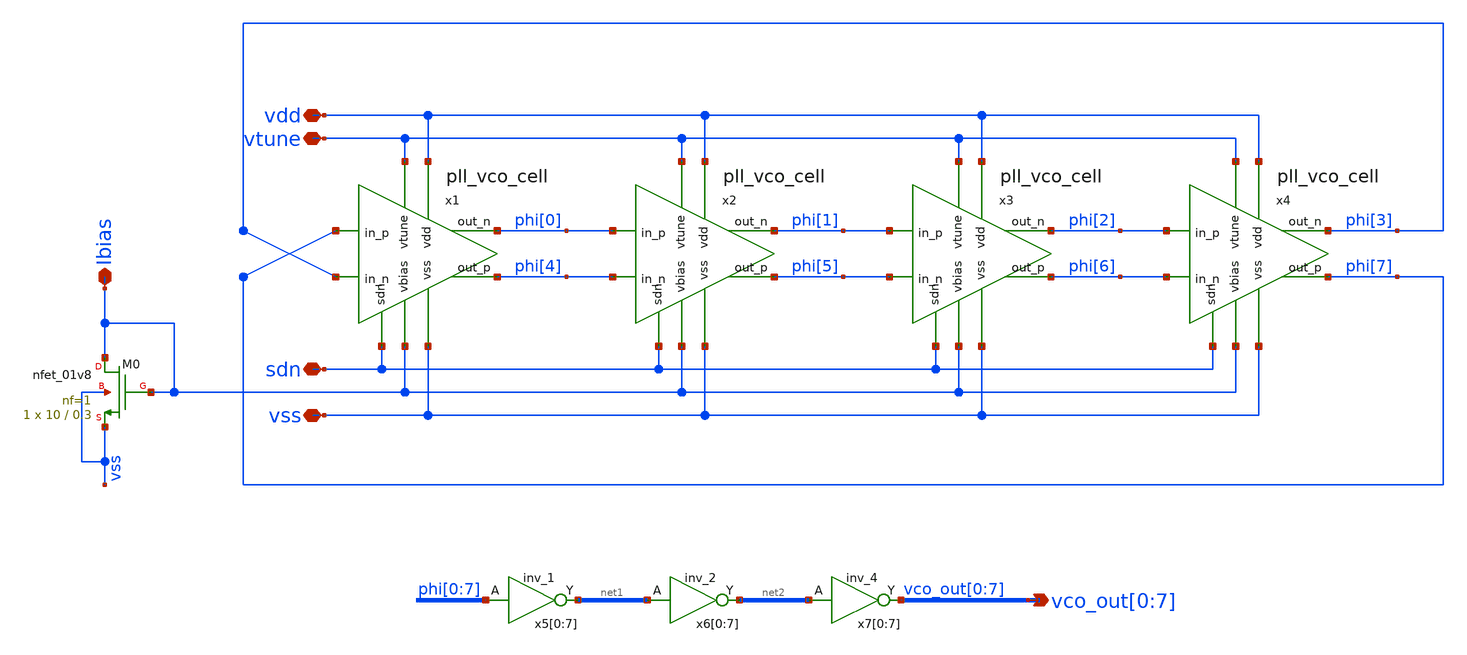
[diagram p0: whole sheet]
** sch_path: pll/pll_vco/xschem/pll_vco.sch
**.subckt pll_vco vss vdd vtune Ibias
*+ vco_out[0],vco_out[1],vco_out[2],vco_out[3],vco_out[4],vco_out[5],vco_out[6],vco_out[7] sdn
*.iopin vss
*.iopin vdd
*.iopin vtune
*.iopin Ibias
*.opin vco_out[0],vco_out[1],vco_out[2],vco_out[3],vco_out[4],vco_out[5],vco_out[6],vco_out[7]
*.iopin sdn
XM0 Ibias Ibias vss vss sky130_fd_pr__nfet_01v8 L=0.3 W=10 nf=1 ad='int((nf+1)/2) * W/nf * 0.29' as='int((nf+2)/2) * W/nf * 0.29'
+ pd='2*int((nf+1)/2) * (W/nf + 0.29)' ps='2*int((nf+2)/2) * (W/nf + 0.29)' nrd='0.29 / W' nrs='0.29 / W'
+ sa=0 sb=0 sd=0 mult=1 m=1
x5[0] phi[0] vss vss vdd vdd net1[7] sky130_fd_sc_hs__inv_1
x5[1] phi[1] vss vss vdd vdd net1[6] sky130_fd_sc_hs__inv_1
x5[2] phi[2] vss vss vdd vdd net1[5] sky130_fd_sc_hs__inv_1
x5[3] phi[3] vss vss vdd vdd net1[4] sky130_fd_sc_hs__inv_1
x5[4] phi[4] vss vss vdd vdd net1[3] sky130_fd_sc_hs__inv_1
x5[5] phi[5] vss vss vdd vdd net1[2] sky130_fd_sc_hs__inv_1
x5[6] phi[6] vss vss vdd vdd net1[1] sky130_fd_sc_hs__inv_1
x5[7] phi[7] vss vss vdd vdd net1[0] sky130_fd_sc_hs__inv_1
x6[0] net1[7] vss vss vdd vdd net2[7] sky130_fd_sc_hs__inv_2
x6[1] net1[6] vss vss vdd vdd net2[6] sky130_fd_sc_hs__inv_2
x6[2] net1[5] vss vss vdd vdd net2[5] sky130_fd_sc_hs__inv_2
x6[3] net1[4] vss vss vdd vdd net2[4] sky130_fd_sc_hs__inv_2
x6[4] net1[3] vss vss vdd vdd net2[3] sky130_fd_sc_hs__inv_2
x6[5] net1[2] vss vss vdd vdd net2[2] sky130_fd_sc_hs__inv_2
x6[6] net1[1] vss vss vdd vdd net2[1] sky130_fd_sc_hs__inv_2
x6[7] net1[0] vss vss vdd vdd net2[0] sky130_fd_sc_hs__inv_2
x7[0] net2[7] vss vss vdd vdd vco_out[0] sky130_fd_sc_hs__inv_4
x7[1] net2[6] vss vss vdd vdd vco_out[1] sky130_fd_sc_hs__inv_4
x7[2] net2[5] vss vss vdd vdd vco_out[2] sky130_fd_sc_hs__inv_4
x7[3] net2[4] vss vss vdd vdd vco_out[3] sky130_fd_sc_hs__inv_4
x7[4] net2[3] vss vss vdd vdd vco_out[4] sky130_fd_sc_hs__inv_4
x7[5] net2[2] vss vss vdd vdd vco_out[5] sky130_fd_sc_hs__inv_4
x7[6] net2[1] vss vss vdd vdd vco_out[6] sky130_fd_sc_hs__inv_4
x7[7] net2[0] vss vss vdd vdd vco_out[7] sky130_fd_sc_hs__inv_4
x1 phi[0] phi[4] phi[7] phi[3] vdd vtune Ibias vss sdn pll_vco_cell
x2 phi[1] phi[5] phi[0] phi[4] vdd vtune Ibias vss sdn pll_vco_cell
x3 phi[2] phi[6] phi[1] phi[5] vdd vtune Ibias vss sdn pll_vco_cell
x4 phi[3] phi[7] phi[2] phi[6] vdd vtune Ibias vss sdn pll_vco_cell
**** begin user architecture code


.control
save i(@m.${path}xm1.msky130_fd_pr__nfet_01v8[id])
save @m.${path}xm1.msky130_fd_pr__nfet_01v8[gm]
save v(@m.${path}xm1.msky130_fd_pr__nfet_01v8[vds])
save v(@m.${path}xm1.msky130_fd_pr__nfet_01v8[vgs])
save v(@m.${path}xm1.msky130_fd_pr__nfet_01v8[vth])
save v(@m.${path}xm1.msky130_fd_pr__nfet_01v8[vdsat])

save i(@m.${path}xm2.msky130_fd_pr__nfet_01v8[id])
save @m.${path}xm2.msky130_fd_pr__nfet_01v8[gm]
save v(@m.${path}xm2.msky130_fd_pr__nfet_01v8[vds])
save v(@m.${path}xm2.msky130_fd_pr__nfet_01v8[vgs])
save v(@m.${path}xm2.msky130_fd_pr__nfet_01v8[vth])
save v(@m.${path}xm2.msky130_fd_pr__nfet_01v8[vdsat])
.endc


**** end user architecture code
**.ends

* expanding   symbol:  pll_vco_cell/xschem/pll_vco_cell.sym # of pins=9
** sym_path: pll/pll_vco_cell/xschem/pll_vco_cell.sym
** sch_path: pll/pll_vco_cell/xschem/pll_vco_cell.sch
.subckt pll_vco_cell out_n out_p in_p in_n vdd vtune vbias vss sdn
*.iopin vss
*.iopin vdd
*.ipin in_p
*.ipin in_n
*.iopin vbias
*.opin out_n
*.opin out_p
*.ipin vtune
*.ipin sdn
**** begin user architecture code


*.control
*save i(@m.${path}xm1.msky130_fd_pr__nfet_01v8[id])
*save @m.${path}xm1.msky130_fd_pr__nfet_01v8[gm]
*save v(@m.${path}xm1.msky130_fd_pr__nfet_01v8[vds])
*save v(@m.${path}xm1.msky130_fd_pr__nfet_01v8[vgs])
*save v(@m.${path}xm1.msky130_fd_pr__nfet_01v8[vth])
*save v(@m.${path}xm1.msky130_fd_pr__nfet_01v8[vdsat])

*save i(@m.${path}xm2.msky130_fd_pr__nfet_01v8[id])
*save @m.${path}xm2.msky130_fd_pr__nfet_01v8[gm]
*save v(@m.${path}xm2.msky130_fd_pr__nfet_01v8[vds])
*save v(@m.${path}xm2.msky130_fd_pr__nfet_01v8[vgs])
*save v(@m.${path}xm2.msky130_fd_pr__nfet_01v8[vth])
*save v(@m.${path}xm2.msky130_fd_pr__nfet_01v8[vdsat])
*.endc


**** end user architecture code
XM3 net1 vbias vss vss sky130_fd_pr__nfet_01v8 L=0.3 W=60 nf=1 ad='int((nf+1)/2) * W/nf * 0.29' as='int((nf+2)/2) * W/nf * 0.29'
+ pd='2*int((nf+1)/2) * (W/nf + 0.29)' ps='2*int((nf+2)/2) * (W/nf + 0.29)' nrd='0.29 / W' nrs='0.29 / W'
+ sa=0 sb=0 sd=0 mult=4 m=4
XM10 vbias sdn vss vss sky130_fd_pr__nfet_01v8 L=0.15 W=0.5 nf=1 ad='int((nf+1)/2) * W/nf * 0.29' as='int((nf+2)/2) * W/nf * 0.29'
+ pd='2*int((nf+1)/2) * (W/nf + 0.29)' ps='2*int((nf+2)/2) * (W/nf + 0.29)' nrd='0.29 / W' nrs='0.29 / W'
+ sa=0 sb=0 sd=0 mult=1 m=1
x1 sdn vss vss vdd vdd net2 sky130_fd_sc_hd__inv_1
x2 sdn vss vss vdd vdd net3 sky130_fd_sc_hd__inv_1
XM4 out_n out_n vdd vdd sky130_fd_pr__pfet_01v8 L=0.15 W=8 nf=1 ad='int((nf+1)/2) * W/nf * 0.29' as='int((nf+2)/2) * W/nf * 0.29'
+ pd='2*int((nf+1)/2) * (W/nf + 0.29)' ps='2*int((nf+2)/2) * (W/nf + 0.29)' nrd='0.29 / W' nrs='0.29 / W'
+ sa=0 sb=0 sd=0 mult=1 m=1
XM5 out_p out_p vdd vdd sky130_fd_pr__pfet_01v8 L=0.15 W=8 nf=1 ad='int((nf+1)/2) * W/nf * 0.29' as='int((nf+2)/2) * W/nf * 0.29'
+ pd='2*int((nf+1)/2) * (W/nf + 0.29)' ps='2*int((nf+2)/2) * (W/nf + 0.29)' nrd='0.29 / W' nrs='0.29 / W'
+ sa=0 sb=0 sd=0 mult=1 m=1
XM7 out_p out_n vdd vdd sky130_fd_pr__pfet_01v8 L=0.15 W=16 nf=1 ad='int((nf+1)/2) * W/nf * 0.29' as='int((nf+2)/2) * W/nf * 0.29'
+ pd='2*int((nf+1)/2) * (W/nf + 0.29)' ps='2*int((nf+2)/2) * (W/nf + 0.29)' nrd='0.29 / W' nrs='0.29 / W'
+ sa=0 sb=0 sd=0 mult=1 m=1
XM6 out_n out_p vdd vdd sky130_fd_pr__pfet_01v8 L=0.15 W=16 nf=1 ad='int((nf+1)/2) * W/nf * 0.29' as='int((nf+2)/2) * W/nf * 0.29'
+ pd='2*int((nf+1)/2) * (W/nf + 0.29)' ps='2*int((nf+2)/2) * (W/nf + 0.29)' nrd='0.29 / W' nrs='0.29 / W'
+ sa=0 sb=0 sd=0 mult=1 m=1
XM8 out_n net2 vdd vdd sky130_fd_pr__pfet_01v8 L=0.15 W=0.5 nf=1 ad='int((nf+1)/2) * W/nf * 0.29' as='int((nf+2)/2) * W/nf * 0.29'
+ pd='2*int((nf+1)/2) * (W/nf + 0.29)' ps='2*int((nf+2)/2) * (W/nf + 0.29)' nrd='0.29 / W' nrs='0.29 / W'
+ sa=0 sb=0 sd=0 mult=1 m=1
XM9 out_p net3 vdd vdd sky130_fd_pr__pfet_01v8 L=0.15 W=0.5 nf=1 ad='int((nf+1)/2) * W/nf * 0.29' as='int((nf+2)/2) * W/nf * 0.29'
+ pd='2*int((nf+1)/2) * (W/nf + 0.29)' ps='2*int((nf+2)/2) * (W/nf + 0.29)' nrd='0.29 / W' nrs='0.29 / W'
+ sa=0 sb=0 sd=0 mult=1 m=1
XM1 out_n in_p net1 vss sky130_fd_pr__nfet_01v8 L=0.15 W=16 nf=1 ad='int((nf+1)/2) * W/nf * 0.29' as='int((nf+2)/2) * W/nf * 0.29'
+ pd='2*int((nf+1)/2) * (W/nf + 0.29)' ps='2*int((nf+2)/2) * (W/nf + 0.29)' nrd='0.29 / W' nrs='0.29 / W'
+ sa=0 sb=0 sd=0 mult=1 m=1
XM2 out_p in_n net1 vss sky130_fd_pr__nfet_01v8 L=0.15 W=16 nf=1 ad='int((nf+1)/2) * W/nf * 0.29' as='int((nf+2)/2) * W/nf * 0.29'
+ pd='2*int((nf+1)/2) * (W/nf + 0.29)' ps='2*int((nf+2)/2) * (W/nf + 0.29)' nrd='0.29 / W' nrs='0.29 / W'
+ sa=0 sb=0 sd=0 mult=1 m=1
XC1 out_n vtune vss sky130_fd_pr__cap_var_lvt W=7 L=4 VM=3 m=3
XC2 out_p vtune vss sky130_fd_pr__cap_var_lvt W=7 L=4 VM=3 m=3
.ends

.end
